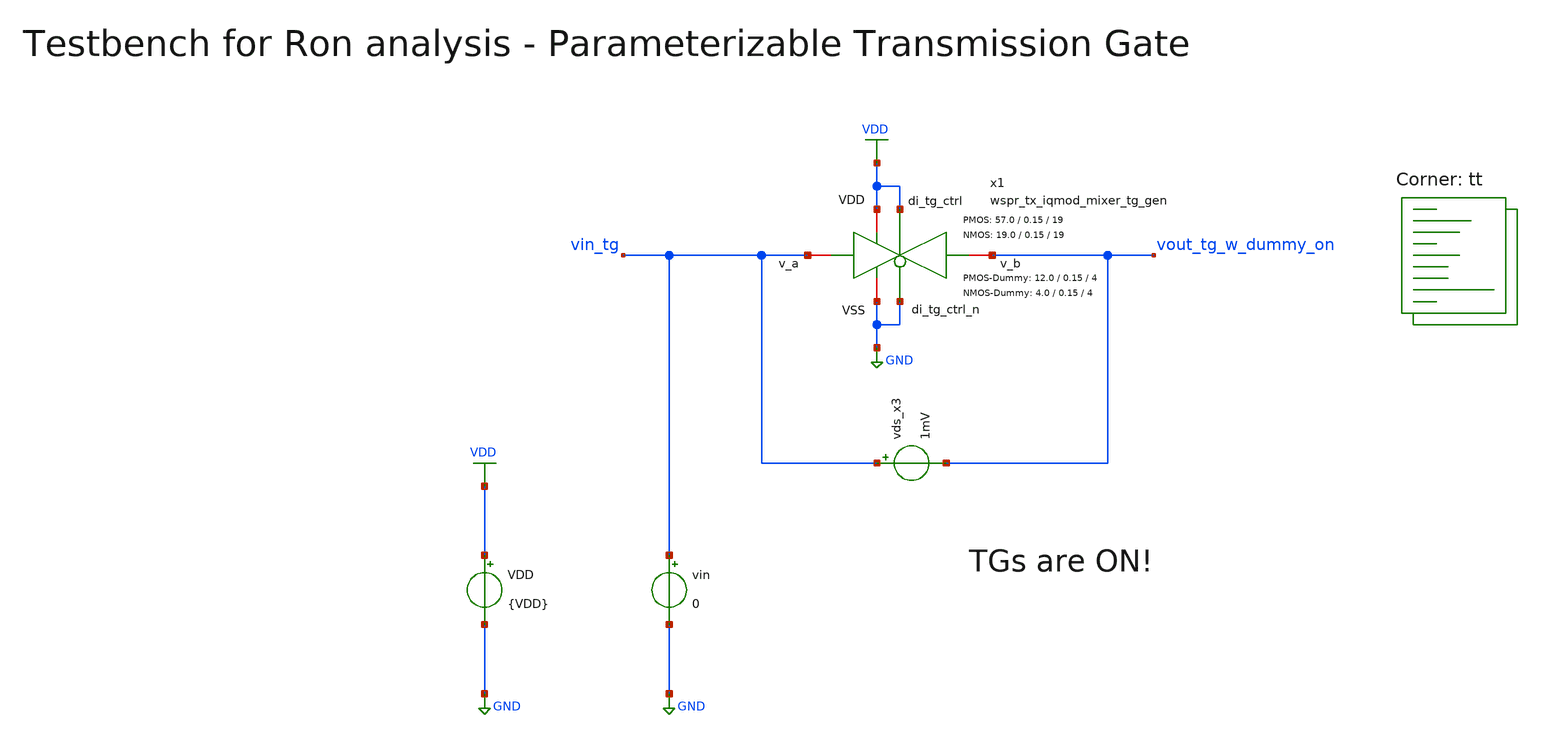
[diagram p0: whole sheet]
** sch_path: sky130/xschem/testbenches/wspr_tx_iqmod_mixer_tg_tb_dc_Ron.sch
**.subckt wspr_tx_iqmod_mixer_tg_tb_dc_Ron
VDD VDD GND {VDD}
vin vin_tg GND 0
vds_x3 vin_tg vout_tg_w_dummy_on 1mV
x1 VDD VDD GND vout_tg_w_dummy_on vin_tg GND wspr_tx_iqmod_mixer_tg_gen W_P=57.0 L_P=0.15 NF_P=19
+ W_N=19.0 L_N=0.15 NF_N=19 W_P_D=12.0 L_P_D=0.15 NF_P_D=4 W_N_D=4.0 L_N_D=0.15 NF_N_D=4
**** begin user architecture code


.param VDD=1.8
.csparam VDD=VDD
.param Vcm=VDD/2
.param temp=27
.param Cload=10p
.options savecurrents klu method=gear reltol=1e-4 abstol=1e-15 gmin=1e-15
.control

save all

* Operating Point Analysis
op
remzerovec
write wspr_tx_iqmod_mixer_tg_tb_dc_Ron.raw
set appendwrite

* DC Sweep Analysis
dc vin 0 $&VDD 0.01
write wspr_tx_iqmod_mixer_tg_tb_dc_Ron.raw

* On-Resistance
* LV with Dummy
let r_w_dummy_on = (v(vout_tg_w_dummy_on)-v(vin_tg))/I(vds_x3)
plot r_w_dummy_on xlabel 'Vin in V' ylabel 'Ron with Dummy in Ohm'

* Writing Data
unset appendwrite
set wr_singlescale
set wr_vecnames
wrdata $PROJECT_PATH/python/plot_simulations/data/wspr_tx_iqmod_mixer_tg_tb_dc_Ron.txt
+ v(r_w_dummy_on)

*quit
.endc

.lib $::SKYWATER_MODELS/sky130.lib.spice tt
**** end user architecture code
**.ends
.GLOBAL GND
.GLOBAL VDD
.end
